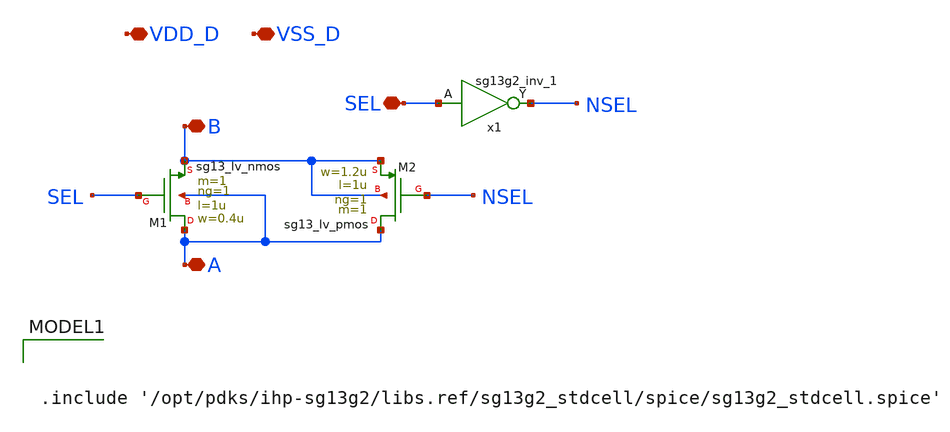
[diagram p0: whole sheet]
** sch_path: Python_layout/transmission_gate/tgate_inv_stdcell.sch
**.subckt tgate_inv_stdcell B SEL A VDD_D VSS_D
*.iopin B
*.iopin SEL
*.iopin A
*.iopin VDD_D
*.iopin VSS_D
XM1 A SEL B A sg13_lv_nmos w=0.4u l=1u ng=1 m=1 mm_ok=1
XM2 A NSEL B B sg13_lv_pmos w=1.2u l=1u ng=1 m=1 mm_ok=1
x1 NSEL SEL VDD_D VSS_D sg13g2_inv_1
**** begin user architecture code


.include '/opt/pdks/ihp-sg13g2/libs.ref/sg13g2_stdcell/spice/sg13g2_stdcell.spice'

**** end user architecture code
**.ends

* expanding   symbol:  sg13g2_stdcells/sg13g2_inv_1.sym # of pins=2
** sym_path: sg13g2_stdcells/sg13g2_inv_1.sym
** sch_path: sg13g2_stdcells/sg13g2_inv_1.sch
.subckt sg13g2_inv_1 Y A VDD VSS
*.opin Y
*.ipin A
*.iopin VDD
*.iopin VSS
XM1 Y A VSS VSS sg13_lv_nmos w=740.00n l=130.00n ng=1 m=1 mm_ok=1
XM2 Y A VDD VDD sg13_lv_pmos w=1.12u l=130.00n ng=1 m=1 mm_ok=1
.ends

.end
